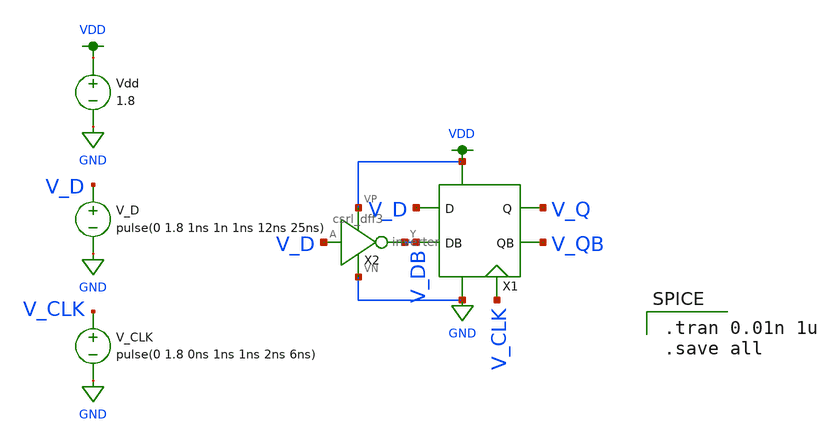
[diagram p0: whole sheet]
** sch_path: MP2/xschem/final/csrl_dff3_tran.sch
**.subckt csrl_dff3_tran
X1 V_D V_DB GND V_CLK V_Q V_QB VDD csrl_dff3
X2 V_D V_DB VDD GND inverter
Vdd VDD GND 1.8
V_D V_D GND pulse(0 1.8 1ns 1n 1ns 12ns 25ns)
V_CLK V_CLK GND pulse(0 1.8 0ns 1ns 1ns 2ns 6ns)
**** begin user architecture code

.tran 0.01n 1u
.save all


.option wnflag=1
.lib ~/skywater/skywater-pdk/libraries/sky130_fd_pr_ngspice/latest/models/sky130.lib.spice sf

**** end user architecture code
**.ends
.GLOBAL GND
.GLOBAL VDD
.end
